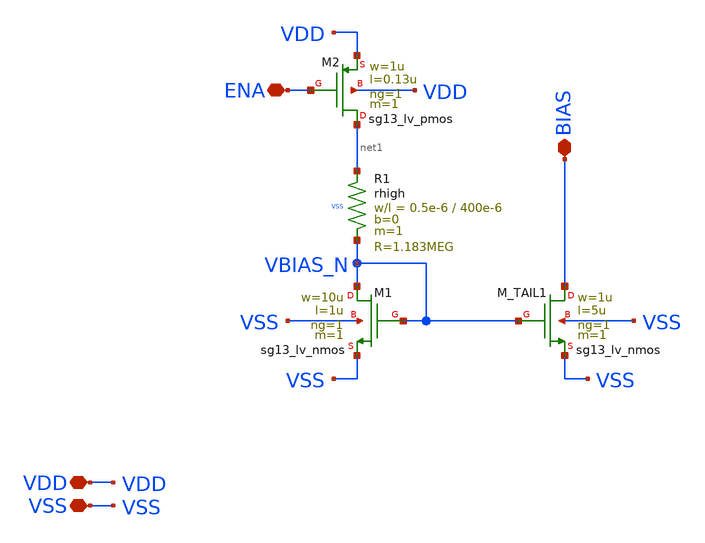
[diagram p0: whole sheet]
** sch_path: xschem/Bias_Gen.sch
**.subckt Bias_Gen VDD VSS BIAS ENA
*.iopin VDD
*.iopin VSS
*.iopin BIAS
*.iopin ENA
XM1 VBIAS_N VBIAS_N VSS VSS sg13_lv_nmos w=10u l=1u ng=1 m=1 mm_ok=1
XM_TAIL1 BIAS VBIAS_N VSS VSS sg13_lv_nmos w=1u l=5u ng=1 m=1 mm_ok=1
XR1 net1 VBIAS_N VSS rhigh w=0.5e-6 l=400e-6 m=1 b=0 mm_ok=1
XM2 net1 ENA VDD VDD sg13_lv_pmos w=1u l=0.13u ng=1 m=1 mm_ok=1
**.ends
.end
